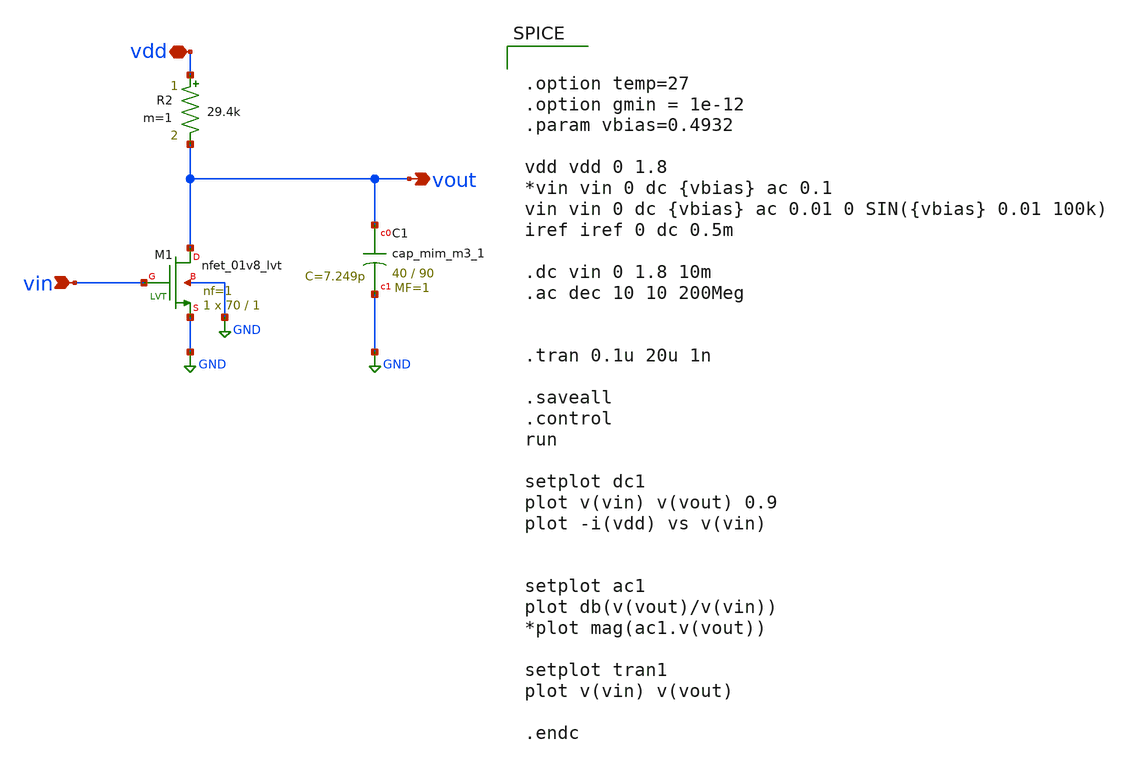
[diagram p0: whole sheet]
** sch_path: src/CS_Resistor.sch
**.subckt CS_Resistor vin vout vdd
*.ipin vin
*.opin vout
*.iopin vdd
XC1 vout GND sky130_fd_pr__cap_mim_m3_1 W=40 L=90 MF=1 m=1
XM1 vout vin GND GND sky130_fd_pr__nfet_01v8_lvt L=1 W=70 nf=1 ad='int((nf+1)/2) * W/nf * 0.29' as='int((nf+2)/2) * W/nf * 0.29'
+ pd='2*int((nf+1)/2) * (W/nf + 0.29)' ps='2*int((nf+2)/2) * (W/nf + 0.29)' nrd='0.29 / W' nrs='0.29 / W'
+ sa=0 sb=0 sd=0 mult=1 m=1
R2 vdd vout 29.4k m=1
**** begin user architecture code

** opencircuitdesign pdks install
.lib $::SKYWATER_MODELS/sky130.lib.spice tt




.option temp=27
.option gmin = 1e-12
.param vbias=0.4932

vdd vdd 0 1.8
*vin vin 0 dc {vbias} ac 0.1
vin vin 0 dc {vbias} ac 0.01 0 SIN({vbias} 0.01 100k)
iref iref 0 dc 0.5m

.dc vin 0 1.8 10m
.ac dec 10 10 200Meg


.tran 0.1u 20u 1n

.saveall
.control
run

setplot dc1
plot v(vin) v(vout) 0.9
plot -i(vdd) vs v(vin)


setplot ac1
plot db(v(vout)/v(vin))
*plot mag(ac1.v(vout))

setplot tran1
plot v(vin) v(vout)

.endc


**** end user architecture code
**.ends
.GLOBAL GND
.end
